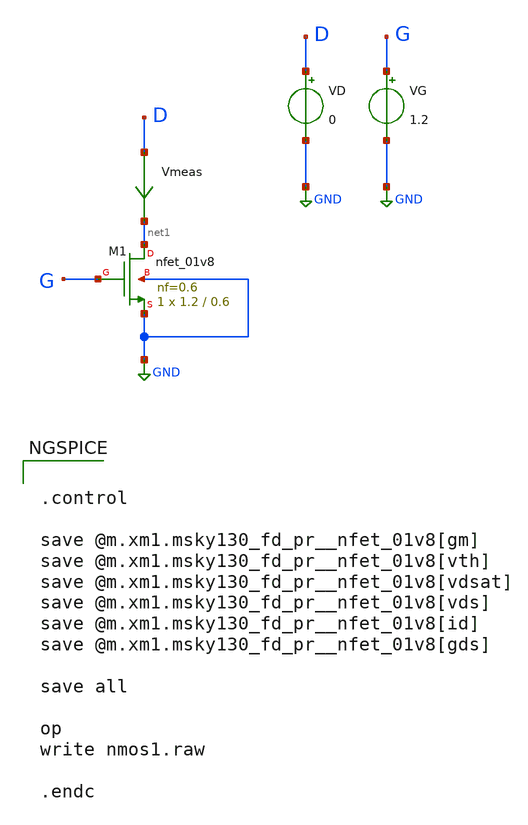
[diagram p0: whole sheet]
** sch_path: nmos-pmos/nmos1.sch
**.subckt nmos1
Vmeas D net1 0
.save i(vmeas)
VD D GND 0
VG G GND 1.2
XM1 net1 G GND GND sky130_fd_pr__nfet_01v8 L=0.6 W=1.2 nf=0.6 ad='int((nf+1)/2) * W/nf * 0.29' as='int((nf+2)/2) * W/nf * 0.29'
+ pd='2*int((nf+1)/2) * (W/nf + 0.29)' ps='2*int((nf+2)/2) * (W/nf + 0.29)' nrd='0.29 / W' nrs='0.29 / W'
+ sa=0 sb=0 sd=0 mult=1 m=1
**** begin user architecture code


.control

save @m.xm1.msky130_fd_pr__nfet_01v8[gm]
save @m.xm1.msky130_fd_pr__nfet_01v8[vth]
save @m.xm1.msky130_fd_pr__nfet_01v8[vdsat]
save @m.xm1.msky130_fd_pr__nfet_01v8[vds]
save @m.xm1.msky130_fd_pr__nfet_01v8[id]
save @m.xm1.msky130_fd_pr__nfet_01v8[gds]

save all

op
write nmos1.raw

.endc



** opencircuitdesign pdks install
.lib $::SKYWATER_MODELS/sky130.lib.spice tt


**** end user architecture code
**.ends
.GLOBAL GND
.end
